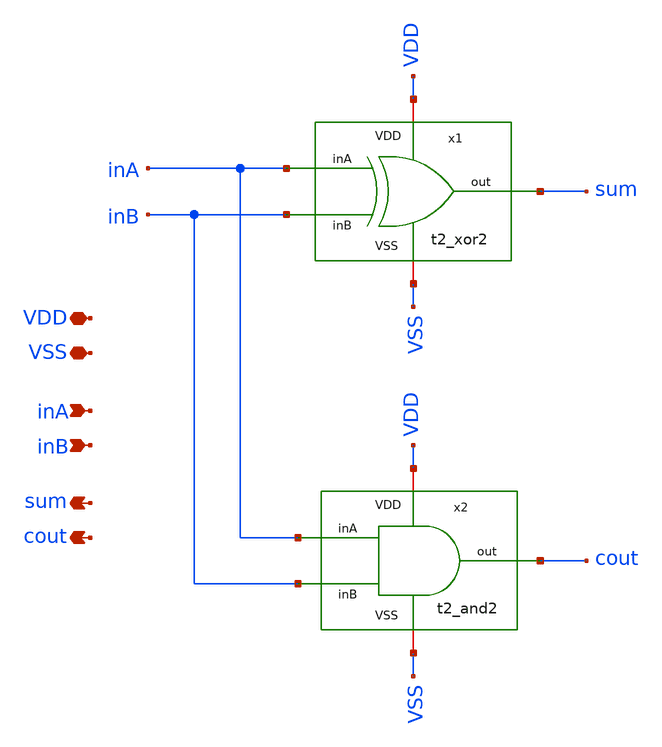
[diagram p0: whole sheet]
** sch_path: Team 2 Design/design_data/xschem/t2_ha.sch
**.subckt t2_ha VSS inA inB sum VDD cout
*.iopin VSS
*.ipin inA
*.ipin inB
*.opin sum
*.iopin VDD
*.opin cout
x1 VDD VSS inA inB sum t2_xor2
x2 VDD VSS inA cout inB t2_and2
**.ends
.end
